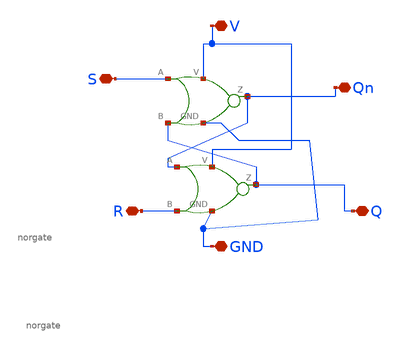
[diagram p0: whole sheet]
** sch_path: SAR_ADC/xschem/spice/SR_nor.sch
**.subckt SR_nor V GND S R Qn Q
*.iopin V
*.iopin GND
*.iopin S
*.iopin R
*.iopin Qn
*.iopin Q
X1 S Q Qn GND V norgate
X2 Qn R Q GND V norgate
**** begin user architecture code

.include /foss/pdks/gf180mcuC/libs.tech/ngspice/design.ngspice
.lib /foss/pdks/gf180mcuC/libs.tech/ngspice/sm141064.ngspice typical

**** end user architecture code
**.ends

* expanding   symbol:  ../spice/norgate.sym # of pins=5
** sym_path: SAR_ADC/xschem/spice/norgate.sym
** sch_path: SAR_ADC/xschem/spice/norgate.sch
.subckt norgate A B Z GND V
*.iopin GND
*.iopin A
*.iopin B
*.iopin V
*.iopin Z
XM3 net2 A V V pfet_03v3 L=0.28u W=0.22u nf=1 ad='int((nf+1)/2) * W/nf * 0.18u' as='int((nf+2)/2) * W/nf * 0.18u'
+ pd='2*int((nf+1)/2) * (W/nf + 0.18u)' ps='2*int((nf+2)/2) * (W/nf + 0.18u)' nrd='0.18u / W' nrs='0.18u / W'
+ sa=0 sb=0 sd=0 m=1
XM6 Z B net2 V pfet_03v3 L=0.28u W=0.22u nf=1 ad='int((nf+1)/2) * W/nf * 0.18u' as='int((nf+2)/2) * W/nf * 0.18u'
+ pd='2*int((nf+1)/2) * (W/nf + 0.18u)' ps='2*int((nf+2)/2) * (W/nf + 0.18u)' nrd='0.18u / W' nrs='0.18u / W'
+ sa=0 sb=0 sd=0 m=1
XM9 net1 B V V pfet_03v3 L=0.28u W=0.22u nf=1 ad='int((nf+1)/2) * W/nf * 0.18u' as='int((nf+2)/2) * W/nf * 0.18u'
+ pd='2*int((nf+1)/2) * (W/nf + 0.18u)' ps='2*int((nf+2)/2) * (W/nf + 0.18u)' nrd='0.18u / W' nrs='0.18u / W'
+ sa=0 sb=0 sd=0 m=1
XM12 Z A net1 V pfet_03v3 L=0.28u W=0.22u nf=1 ad='int((nf+1)/2) * W/nf * 0.18u' as='int((nf+2)/2) * W/nf * 0.18u'
+ pd='2*int((nf+1)/2) * (W/nf + 0.18u)' ps='2*int((nf+2)/2) * (W/nf + 0.18u)' nrd='0.18u / W' nrs='0.18u / W'
+ sa=0 sb=0 sd=0 m=1
XM2 Z B GND GND nfet_03v3 L=0.28u W=0.22u nf=1 ad='int((nf+1)/2) * W/nf * 0.18u' as='int((nf+2)/2) * W/nf * 0.18u'
+ pd='2*int((nf+1)/2) * (W/nf + 0.18u)' ps='2*int((nf+2)/2) * (W/nf + 0.18u)' nrd='0.18u / W' nrs='0.18u / W'
+ sa=0 sb=0 sd=0 m=1
XM4 Z A GND GND nfet_03v3 L=0.28u W=0.22u nf=1 ad='int((nf+1)/2) * W/nf * 0.18u' as='int((nf+2)/2) * W/nf * 0.18u'
+ pd='2*int((nf+1)/2) * (W/nf + 0.18u)' ps='2*int((nf+2)/2) * (W/nf + 0.18u)' nrd='0.18u / W' nrs='0.18u / W'
+ sa=0 sb=0 sd=0 m=1
.ends

.end
